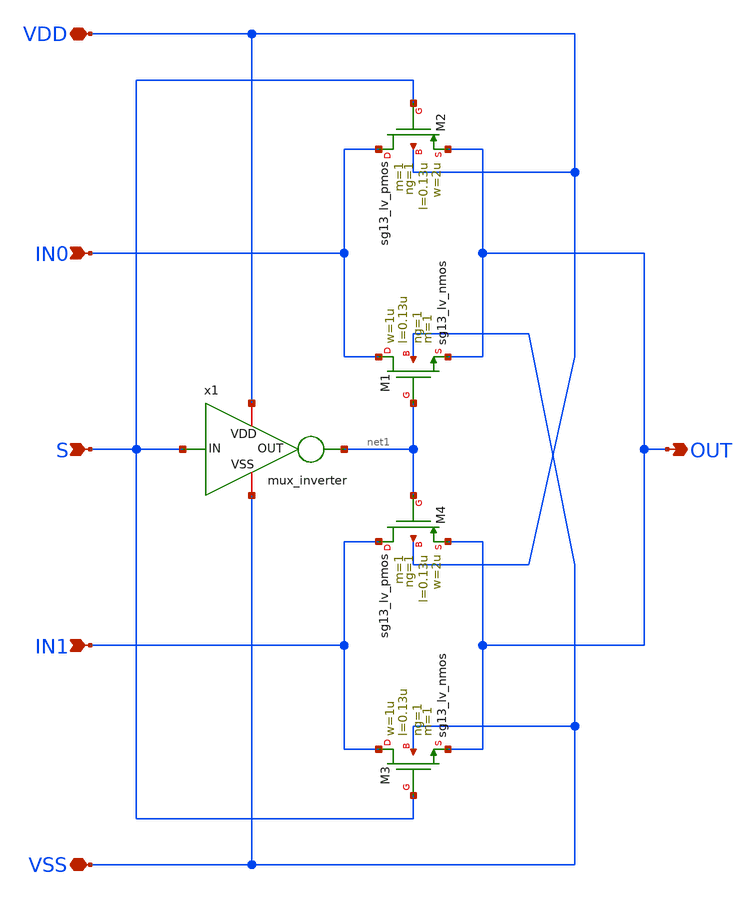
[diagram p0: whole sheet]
** sch_path: SSDOR_1.2V_v4/components/mux/mux.sch
**.subckt mux S IN0 IN1 OUT VDD VSS
*.ipin S
*.ipin IN0
*.ipin IN1
*.opin OUT
*.iopin VDD
*.iopin VSS
XM1 IN0 net1 OUT VSS sg13_lv_nmos w=1u l=0.13u ng=1 m=1 mm_ok=1
XM2 IN0 S OUT VDD sg13_lv_pmos w=2u l=0.13u ng=1 m=1 mm_ok=1
XM3 IN1 S OUT VSS sg13_lv_nmos w=1u l=0.13u ng=1 m=1 mm_ok=1
XM4 IN1 net1 OUT VDD sg13_lv_pmos w=2u l=0.13u ng=1 m=1 mm_ok=1
x1 VSS S net1 VDD mux_inverter
**.ends
.end
